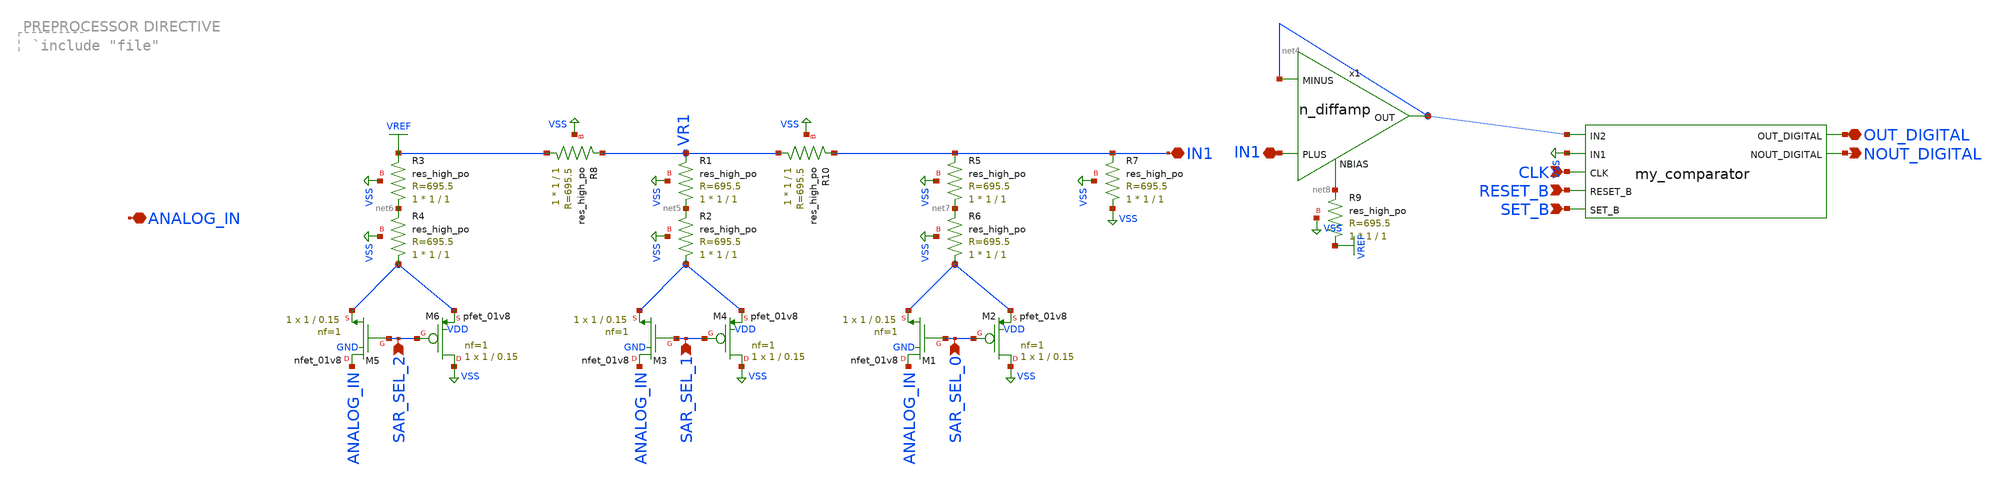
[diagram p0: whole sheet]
** sch_path: 1bit_adc/3bit_dac.sch
* StefanSchippers/xschem_sky130/sky130_tests/n_diffamp.sch:
* Copyright 2021 Stefan Frederik Schippers
* Licensed under the Apache License, Version 2.0 (the "License");
**.subckt 3bit_dac ANALOG_IN SAR_SEL_0 SAR_SEL_1 SAR_SEL_2 IN1 OUT_DIGITAL NOUT_DIGITAL CLK RESET_B
*+ SET_B IN1
*.iopin ANALOG_IN
*.ipin SAR_SEL_0
*.ipin SAR_SEL_1
*.ipin SAR_SEL_2
*.iopin IN1
*.iopin OUT_DIGITAL
*.opin NOUT_DIGITAL
*.ipin CLK
*.ipin RESET_B
*.ipin SET_B
*.iopin IN1
XM1 ANALOG_IN SAR_SEL_0 net1 GND sky130_fd_pr__nfet_01v8 L=0.15 W=1 nf=1 ad='int((nf+1)/2) * W/nf * 0.29'
+ as='int((nf+2)/2) * W/nf * 0.29' pd='2*int((nf+1)/2) * (W/nf + 0.29)' ps='2*int((nf+2)/2) * (W/nf + 0.29)'
+ nrd='0.29 / W' nrs='0.29 / W' sa=0 sb=0 sd=0 mult=1 m=1
XM2 VSS SAR_SEL_0 net1 VDD sky130_fd_pr__pfet_01v8 L=0.15 W=1 nf=1 ad='int((nf+1)/2) * W/nf * 0.29' as='int((nf+2)/2) * W/nf * 0.29'
+ pd='2*int((nf+1)/2) * (W/nf + 0.29)' ps='2*int((nf+2)/2) * (W/nf + 0.29)' nrd='0.29 / W' nrs='0.29 / W'
+ sa=0 sb=0 sd=0 mult=1 m=1
XM3 ANALOG_IN SAR_SEL_1 net2 GND sky130_fd_pr__nfet_01v8 L=0.15 W=1 nf=1 ad='int((nf+1)/2) * W/nf * 0.29'
+ as='int((nf+2)/2) * W/nf * 0.29' pd='2*int((nf+1)/2) * (W/nf + 0.29)' ps='2*int((nf+2)/2) * (W/nf + 0.29)'
+ nrd='0.29 / W' nrs='0.29 / W' sa=0 sb=0 sd=0 mult=1 m=1
XM4 VSS SAR_SEL_1 net2 VDD sky130_fd_pr__pfet_01v8 L=0.15 W=1 nf=1 ad='int((nf+1)/2) * W/nf * 0.29' as='int((nf+2)/2) * W/nf * 0.29'
+ pd='2*int((nf+1)/2) * (W/nf + 0.29)' ps='2*int((nf+2)/2) * (W/nf + 0.29)' nrd='0.29 / W' nrs='0.29 / W'
+ sa=0 sb=0 sd=0 mult=1 m=1
XM5 ANALOG_IN SAR_SEL_2 net3 GND sky130_fd_pr__nfet_01v8 L=0.15 W=1 nf=1 ad='int((nf+1)/2) * W/nf * 0.29'
+ as='int((nf+2)/2) * W/nf * 0.29' pd='2*int((nf+1)/2) * (W/nf + 0.29)' ps='2*int((nf+2)/2) * (W/nf + 0.29)'
+ nrd='0.29 / W' nrs='0.29 / W' sa=0 sb=0 sd=0 mult=1 m=1
XM6 VSS SAR_SEL_2 net3 VDD sky130_fd_pr__pfet_01v8 L=0.15 W=1 nf=1 ad='int((nf+1)/2) * W/nf * 0.29' as='int((nf+2)/2) * W/nf * 0.29'
+ pd='2*int((nf+1)/2) * (W/nf + 0.29)' ps='2*int((nf+2)/2) * (W/nf + 0.29)' nrd='0.29 / W' nrs='0.29 / W'
+ sa=0 sb=0 sd=0 mult=1 m=1
XR10 VR1 IN1 VSS sky130_fd_pr__res_high_po W=1 L=1 mult=1 m=1
XR1 net5 VR1 VSS sky130_fd_pr__res_high_po W=1 L=1 mult=1 m=1
XR2 net2 net5 VSS sky130_fd_pr__res_high_po W=1 L=1 mult=1 m=1
XR3 net6 VREF VSS sky130_fd_pr__res_high_po W=1 L=1 mult=1 m=1
XR4 net3 net6 VSS sky130_fd_pr__res_high_po W=1 L=1 mult=1 m=1
XR5 net7 IN1 VSS sky130_fd_pr__res_high_po W=1 L=1 mult=1 m=1
XR6 net1 net7 VSS sky130_fd_pr__res_high_po W=1 L=1 mult=1 m=1
XR7 VSS IN1 VSS sky130_fd_pr__res_high_po W=1 L=1 mult=1 m=1
XR8 VREF VR1 VSS sky130_fd_pr__res_high_po W=1 L=1 mult=1 m=1
x1 net4 net4 IN1 net8 n_diffamp
XR9 VREF net8 VSS sky130_fd_pr__res_high_po W=1 L=1 mult=1 m=1
**** begin user architecture code



.options gmin=1e-12
.option savecurrents
.option wnflag=1

.param vdd=1.8
.param clk=300n

VVDD VDD 0 DC {vdd}
VCLK CLK 0 PULSE(0 {vdd} 0 {clk/10} {clk/10} {1.5*clk} {2*clk})
VVSS VSS 0 DC 0
VVREF VREF 0 DC 3
VANALOG_IN 0 DC 0.9
VSET_B SET_B 0 DC {vdd}
VRESET_B RESET_B 0 DC {vdd}
*VSAR_SEL_2 SAR_SEL_2 0 0
*VSAR_SEL_1 SAR_SEL_1 0 0
*VSAR_SEL_0 SAR_SEL_0 0 0

*VANALOG_IN ANALOG_IN 0 pwl(0 0  0.5u 0.1  1u 0.2  1.5u 0.3  2u 0.4  2.5u 0.5  3u 0.6  3.5u 0.7  4u
*+ 0.8  4.5u 0.9  5u 1.0  5.5u 1.1  6u 1.2  6.5u 1.3  7u 1.4  7.5u 1.5  8u 1.6  8.5u 1.7  9u 1.8  9.5u 0
*+  10u 0.1  10.5u 0.2  11u 0.3  11.5u 0.4  12u 0.5  12.5u 0.6  13u 0.7  13.5u 0.8  14u 0.9  14.5u 1.0  15u
*+ 1.1  15.5u 1.2  16u 1.3  16.5u 1.4  17u 1.5  17.5u 1.6  18u 1.7  18.5u 1.8  19u 0)
* Bit 0 (LSB) - period = 2us, toggles every 1us
VSAR_SEL_2 SAR_SEL_2 0 pwl(0 0  1u 0  1.1u 1.8  2u 1.8  2.1u 0  3u 0  3.1u 1.8  4u 1.8  4.1u 0  5u 0
+  5.1u 1.8  6u 1.8  6.1u 0  7u 0  7.1u 1.8  8u 1.8  8.1u 0  9u 0  9.1u 1.8  10u 1.8  10.1u 0  11u 0  11.1u
+ 1.8  12u 1.8  12.1u 0  13u 0  13.1u 1.8  14u 1.8  14.1u 0  15u 0  15.1u 1.8  16u 1.8  16.1u 0  17u 0
+  17.1u 1.8  18u 1.8  18.1u 0  19u 0  19.1u 1.8  20u 1.8  20.1u 0  21u 0  21.1u 1.8  22u 1.8  22.1u 0  23u
+ 0  23.1u 1.8  24u 1.8  24.1u 0  25u 0  25.1u 1.8  26u 1.8  26.1u 0  27u 0  27.1u 1.8  28u 1.8  28.1u
+ 0  29u 0  29.1u 1.8  30u 1.8  30.1u 0  31u 0  31.1u 1.8  32u 1.8)
* Bit 1 - period = 4us, toggles every 2us
VSAR_SEL_1 SAR_SEL_1 0 pwl(0 0  2u 0  2.1u 1.8  4u 1.8  4.1u 0  6u 0  6.1u 1.8  8u 1.8  8.1u 0  10u
+ 0  10.1u 1.8  12u 1.8  12.1u 0  14u 0  14.1u 1.8  16u 1.8  16.1u 0  18u 0  18.1u 1.8  20u 1.8  20.1u
+ 0  22u 0  22.1u 1.8  24u 1.8  24.1u 0  26u 0  26.1u 1.8  28u 1.8  28.1u 0  30u 0  30.1u 1.8  32u 1.8)
* Bit 2 - period = 8us, toggles every 4us
VSAR_SEL_0 SAR_SEL_0 0 pwl(0 0  4u 0  4.1u 1.8  8u 1.8  8.1u 0  12u 0  12.1u 1.8  16u 1.8  16.1u 0
+  20u 0  20.1u 1.8  24u 1.8  24.1u 0  28u 0  28.1u 1.8  32u 1.8)
* Bit 3 (MSB) - period = 16us, toggles every 8us
VEN EN 0 pwl(0 0  8u 0  8.1u 1.8  16u 1.8  16.1u 0  24u 0  24.1u 1.8  32u 1.8)


.tran {clk/4} {clk*300}
.control

save all
echo TRAN
run
write 3bit_dac.raw all

.endc
.end



** opencircuitdesign pdks install
.lib $::SKYWATER_MODELS/sky130.lib.spice tt
.include $::SKYWATER_STDCELLS/sky130_fd_sc_hd.spice
.include /foss/pdks/sky130A/libs.tech/xschem/sky130_stdcells/

**** end user architecture code
**.ends

* expanding   symbol:  sky130_tests/n_diffamp.sym # of pins=4
** sym_path: sky130_tests/n_diffamp.sym
** sch_path: sky130_tests/n_diffamp.sch
.subckt n_diffamp OUT MINUS PLUS NBIAS
*.ipin PLUS
*.ipin MINUS
*.opin OUT
*.ipin NBIAS
XM1 net1 PLUS S GND sky130_fd_pr__nfet_01v8_lvt L=0.3 W=2 nf=1 ad='int((1 + 1)/2) * 2 / 1 * 0.29' as='int((1 + 2)/2) * 2 / 1 * 0.29'
+ pd='2*int((1 + 1)/2) * (2 / 1 + 0.29)' ps='2*int((1 + 2)/2) * (2 / 1 + 0.29)' nrd='0.29 / 2 ' nrs='0.29 / 2 '
+ sa=0 sb=0 sd=0 mult=1 m=1
XM2 OUT MINUS S GND sky130_fd_pr__nfet_01v8_lvt L=0.3 W=2 nf=1 ad='int((1 + 1)/2) * 2 / 1 * 0.29' as='int((1 + 2)/2) * 2 / 1 * 0.29'
+ pd='2*int((1 + 1)/2) * (2 / 1 + 0.29)' ps='2*int((1 + 2)/2) * (2 / 1 + 0.29)' nrd='0.29 / 2 ' nrs='0.29 / 2 '
+ sa=0 sb=0 sd=0 mult=1 m=1
XM3 OUT net1 VDD VDD sky130_fd_pr__pfet_01v8_lvt L=0.8 W=4 nf=1 ad='int((1 + 1)/2) * 4 / 1 * 0.29' as='int((1 + 2)/2) * 4 / 1 * 0.29'
+ pd='2*int((1 + 1)/2) * (4 / 1 + 0.29)' ps='2*int((1 + 2)/2) * (4 / 1 + 0.29)' nrd='0.29 / 4 ' nrs='0.29 / 4 '
+ sa=0 sb=0 sd=0 mult=1 m=1
XM4 net1 net1 VDD VDD sky130_fd_pr__pfet_01v8_lvt L=0.8 W=4 nf=1 ad='int((1 + 1)/2) * 4 / 1 * 0.29' as='int((1 + 2)/2) * 4 / 1 * 0.29'
+ pd='2*int((1 + 1)/2) * (4 / 1 + 0.29)' ps='2*int((1 + 2)/2) * (4 / 1 + 0.29)' nrd='0.29 / 4 ' nrs='0.29 / 4 '
+ sa=0 sb=0 sd=0 mult=1 m=1
XM5 net2 NBIAS GND GND sky130_fd_pr__nfet_01v8 L=2 W=0.7 nf=1 ad='int((nf+1)/2) * W/nf * 0.29' as='int((nf+2)/2) * W/nf * 0.29'
+ pd='2*int((nf+1)/2) * (W/nf + 0.29)' ps='2*int((nf+2)/2) * (W/nf + 0.29)' nrd='0.29 / W' nrs='0.29 / W'
+ sa=0 sb=0 sd=0 mult=1 m=1
XR1 GND S GND sky130_fd_pr__res_xhigh_po_0p35 L=50 mult=1 m=1
V5 S net2 0
.save i(v5)
.ends

.GLOBAL VSS
.GLOBAL VREF
.GLOBAL GND
.GLOBAL VDD
.end
